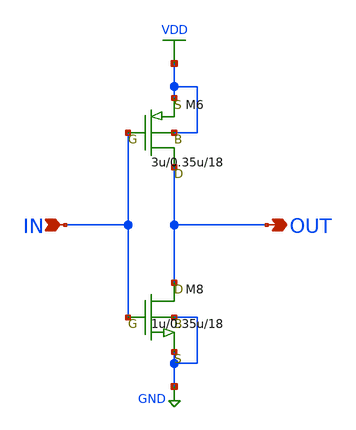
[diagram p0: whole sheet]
** sch_path: LR_hasegawa/LR_Work2/symbol/INVERTER18.sch
**.subckt INVERTER18 OUT IN
*.opin OUT
*.ipin IN
M6 OUT IN VDD VDD pch w=3u l=0.35u as=5.6p ps=9u ad=5.6p pd=9u m=18
M8 OUT IN GND GND nch w=1u l=0.35u as=2.8p ps=5.5u ad=2.8p pd=5.5u m=18
**.ends
.GLOBAL VDD
.GLOBAL GND
.end
